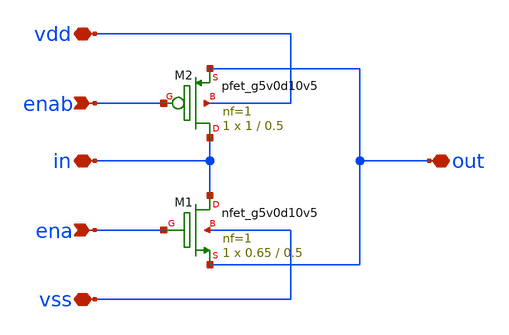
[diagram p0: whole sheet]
** sch_path: xschem/passtrans.sch
**.subckt passtrans enab ena vss vdd in out
*.ipin enab
*.ipin ena
*.iopin vss
*.iopin vdd
*.iopin in
*.iopin out
XM1 in ena out vss sky130_fd_pr__nfet_g5v0d10v5 L=0.5 W=0.65 nf=1 ad='int((nf+1)/2) * W/nf * 0.29' as='int((nf+2)/2) * W/nf * 0.29'
+ pd='2*int((nf+1)/2) * (W/nf + 0.29)' ps='2*int((nf+2)/2) * (W/nf + 0.29)' nrd='0.29 / W' nrs='0.29 / W'
+ sa=0 sb=0 sd=0 mult=1 m=1
XM2 in enab out vdd sky130_fd_pr__pfet_g5v0d10v5 L=0.5 W=1 nf=1 ad='int((nf+1)/2) * W/nf * 0.29' as='int((nf+2)/2) * W/nf * 0.29'
+ pd='2*int((nf+1)/2) * (W/nf + 0.29)' ps='2*int((nf+2)/2) * (W/nf + 0.29)' nrd='0.29 / W' nrs='0.29 / W'
+ sa=0 sb=0 sd=0 mult=1 m=1
**.ends
.end
